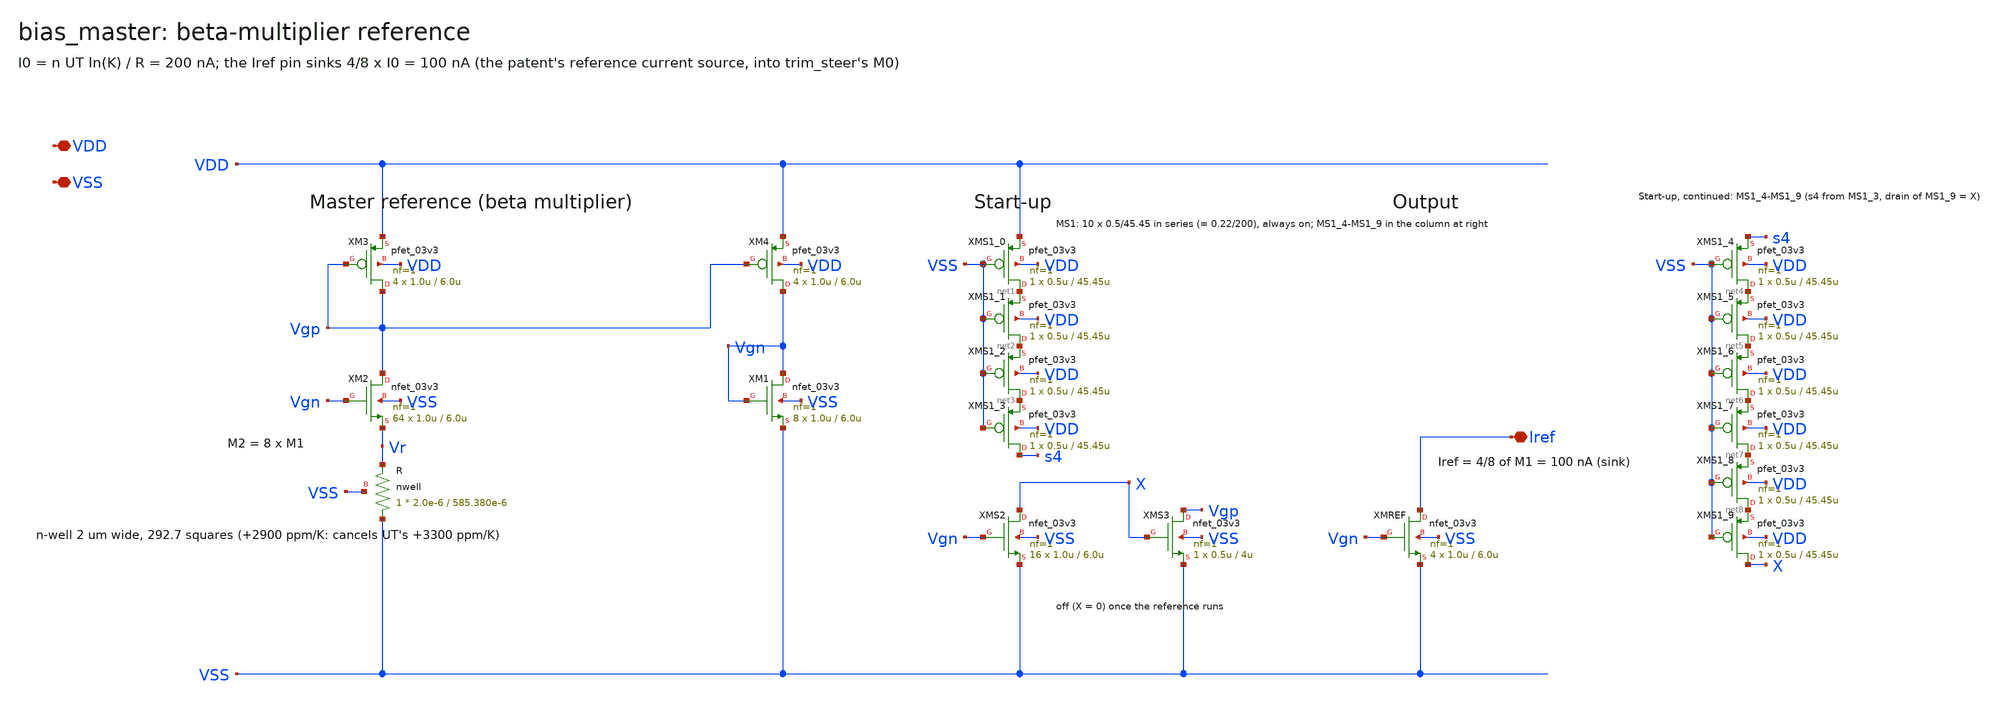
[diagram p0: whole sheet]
** sch_path: analog/bias/generator/bias_master.sch
**.subckt bias_master VDD VSS Iref
*.iopin VDD
*.iopin VSS
*.iopin Iref
XM3 Vgp Vgp VDD VDD pfet_03v3 L=6.0u W=1.0u nf=1 ad='int((nf+1)/2) * W/nf * 0.18u' as='int((nf+2)/2) * W/nf * 0.18u'
+ pd='2*int((nf+1)/2) * (W/nf + 0.18u)' ps='2*int((nf+2)/2) * (W/nf + 0.18u)' nrd='0.18u / W' nrs='0.18u / W'
+ sa=0 sb=0 sd=0 m=4
XM4 Vgn Vgp VDD VDD pfet_03v3 L=6.0u W=1.0u nf=1 ad='int((nf+1)/2) * W/nf * 0.18u' as='int((nf+2)/2) * W/nf * 0.18u'
+ pd='2*int((nf+1)/2) * (W/nf + 0.18u)' ps='2*int((nf+2)/2) * (W/nf + 0.18u)' nrd='0.18u / W' nrs='0.18u / W'
+ sa=0 sb=0 sd=0 m=4
XM2 Vgp Vgn Vr VSS nfet_03v3 L=6.0u W=1.0u nf=1 ad='int((nf+1)/2) * W/nf * 0.18u' as='int((nf+2)/2) * W/nf * 0.18u'
+ pd='2*int((nf+1)/2) * (W/nf + 0.18u)' ps='2*int((nf+2)/2) * (W/nf + 0.18u)' nrd='0.18u / W' nrs='0.18u / W'
+ sa=0 sb=0 sd=0 m=64
XM1 Vgn Vgn VSS VSS nfet_03v3 L=6.0u W=1.0u nf=1 ad='int((nf+1)/2) * W/nf * 0.18u' as='int((nf+2)/2) * W/nf * 0.18u'
+ pd='2*int((nf+1)/2) * (W/nf + 0.18u)' ps='2*int((nf+2)/2) * (W/nf + 0.18u)' nrd='0.18u / W' nrs='0.18u / W'
+ sa=0 sb=0 sd=0 m=8
XR VSS Vr VSS nwell r_width=2.0e-6 r_length=585.380e-6 m=1
XMS1_0 net1 VSS VDD VDD pfet_03v3 L=45.45u W=0.5u nf=1 ad='int((nf+1)/2) * W/nf * 0.18u' as='int((nf+2)/2) * W/nf * 0.18u'
+ pd='2*int((nf+1)/2) * (W/nf + 0.18u)' ps='2*int((nf+2)/2) * (W/nf + 0.18u)' nrd='0.18u / W' nrs='0.18u / W'
+ sa=0 sb=0 sd=0 m=1
XMS1_1 net2 VSS net1 VDD pfet_03v3 L=45.45u W=0.5u nf=1 ad='int((nf+1)/2) * W/nf * 0.18u' as='int((nf+2)/2) * W/nf * 0.18u'
+ pd='2*int((nf+1)/2) * (W/nf + 0.18u)' ps='2*int((nf+2)/2) * (W/nf + 0.18u)' nrd='0.18u / W' nrs='0.18u / W'
+ sa=0 sb=0 sd=0 m=1
XMS1_2 net3 VSS net2 VDD pfet_03v3 L=45.45u W=0.5u nf=1 ad='int((nf+1)/2) * W/nf * 0.18u' as='int((nf+2)/2) * W/nf * 0.18u'
+ pd='2*int((nf+1)/2) * (W/nf + 0.18u)' ps='2*int((nf+2)/2) * (W/nf + 0.18u)' nrd='0.18u / W' nrs='0.18u / W'
+ sa=0 sb=0 sd=0 m=1
XMS1_3 s4 VSS net3 VDD pfet_03v3 L=45.45u W=0.5u nf=1 ad='int((nf+1)/2) * W/nf * 0.18u' as='int((nf+2)/2) * W/nf * 0.18u'
+ pd='2*int((nf+1)/2) * (W/nf + 0.18u)' ps='2*int((nf+2)/2) * (W/nf + 0.18u)' nrd='0.18u / W' nrs='0.18u / W'
+ sa=0 sb=0 sd=0 m=1
XMS2 X Vgn VSS VSS nfet_03v3 L=6.0u W=1.0u nf=1 ad='int((nf+1)/2) * W/nf * 0.18u' as='int((nf+2)/2) * W/nf * 0.18u'
+ pd='2*int((nf+1)/2) * (W/nf + 0.18u)' ps='2*int((nf+2)/2) * (W/nf + 0.18u)' nrd='0.18u / W' nrs='0.18u / W'
+ sa=0 sb=0 sd=0 m=16
XMS3 Vgp X VSS VSS nfet_03v3 L=4u W=0.5u nf=1 ad='int((nf+1)/2) * W/nf * 0.18u' as='int((nf+2)/2) * W/nf * 0.18u'
+ pd='2*int((nf+1)/2) * (W/nf + 0.18u)' ps='2*int((nf+2)/2) * (W/nf + 0.18u)' nrd='0.18u / W' nrs='0.18u / W'
+ sa=0 sb=0 sd=0 m=1
XMREF Iref Vgn VSS VSS nfet_03v3 L=6.0u W=1.0u nf=1 ad='int((nf+1)/2) * W/nf * 0.18u' as='int((nf+2)/2) * W/nf * 0.18u'
+ pd='2*int((nf+1)/2) * (W/nf + 0.18u)' ps='2*int((nf+2)/2) * (W/nf + 0.18u)' nrd='0.18u / W' nrs='0.18u / W'
+ sa=0 sb=0 sd=0 m=4
XMS1_4 net4 VSS s4 VDD pfet_03v3 L=45.45u W=0.5u nf=1 ad='int((nf+1)/2) * W/nf * 0.18u' as='int((nf+2)/2) * W/nf * 0.18u'
+ pd='2*int((nf+1)/2) * (W/nf + 0.18u)' ps='2*int((nf+2)/2) * (W/nf + 0.18u)' nrd='0.18u / W' nrs='0.18u / W'
+ sa=0 sb=0 sd=0 m=1
XMS1_5 net5 VSS net4 VDD pfet_03v3 L=45.45u W=0.5u nf=1 ad='int((nf+1)/2) * W/nf * 0.18u' as='int((nf+2)/2) * W/nf * 0.18u'
+ pd='2*int((nf+1)/2) * (W/nf + 0.18u)' ps='2*int((nf+2)/2) * (W/nf + 0.18u)' nrd='0.18u / W' nrs='0.18u / W'
+ sa=0 sb=0 sd=0 m=1
XMS1_6 net6 VSS net5 VDD pfet_03v3 L=45.45u W=0.5u nf=1 ad='int((nf+1)/2) * W/nf * 0.18u' as='int((nf+2)/2) * W/nf * 0.18u'
+ pd='2*int((nf+1)/2) * (W/nf + 0.18u)' ps='2*int((nf+2)/2) * (W/nf + 0.18u)' nrd='0.18u / W' nrs='0.18u / W'
+ sa=0 sb=0 sd=0 m=1
XMS1_7 net7 VSS net6 VDD pfet_03v3 L=45.45u W=0.5u nf=1 ad='int((nf+1)/2) * W/nf * 0.18u' as='int((nf+2)/2) * W/nf * 0.18u'
+ pd='2*int((nf+1)/2) * (W/nf + 0.18u)' ps='2*int((nf+2)/2) * (W/nf + 0.18u)' nrd='0.18u / W' nrs='0.18u / W'
+ sa=0 sb=0 sd=0 m=1
XMS1_8 net8 VSS net7 VDD pfet_03v3 L=45.45u W=0.5u nf=1 ad='int((nf+1)/2) * W/nf * 0.18u' as='int((nf+2)/2) * W/nf * 0.18u'
+ pd='2*int((nf+1)/2) * (W/nf + 0.18u)' ps='2*int((nf+2)/2) * (W/nf + 0.18u)' nrd='0.18u / W' nrs='0.18u / W'
+ sa=0 sb=0 sd=0 m=1
XMS1_9 X VSS net8 VDD pfet_03v3 L=45.45u W=0.5u nf=1 ad='int((nf+1)/2) * W/nf * 0.18u' as='int((nf+2)/2) * W/nf * 0.18u'
+ pd='2*int((nf+1)/2) * (W/nf + 0.18u)' ps='2*int((nf+2)/2) * (W/nf + 0.18u)' nrd='0.18u / W' nrs='0.18u / W'
+ sa=0 sb=0 sd=0 m=1
**.ends
.end
